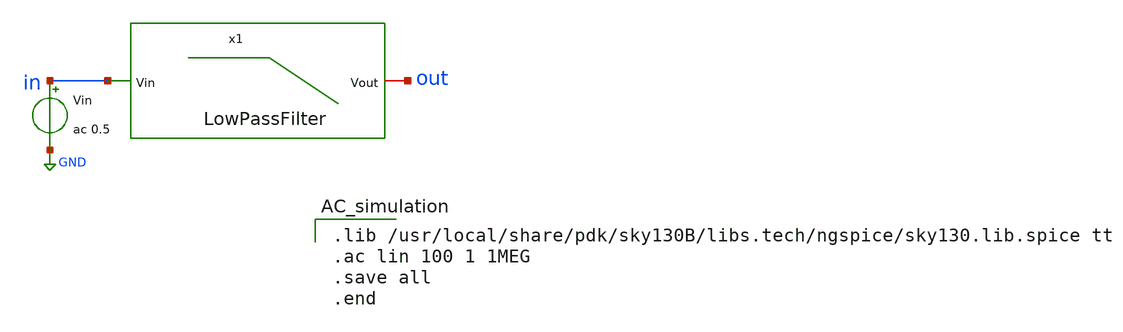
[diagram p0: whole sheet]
** sch_path: xschem/analog_desing/Filtro/LowPassFilter_tb.sch
**.subckt LowPassFilter_tb
x1 out in LowPassFilter
Vin in GND ac 0.5
**** begin user architecture code

.lib /usr/local/share/pdk/sky130B/libs.tech/ngspice/sky130.lib.spice tt
.ac lin 100 1 1MEG
.save all
.end

**** end user architecture code
**.ends

* expanding   symbol:  LowPassFilter.sym # of pins=2
** sym_path: xschem/analog_desing/Filtro/LowPassFilter.sym
** sch_path: xschem/analog_desing/Filtro/LowPassFilter.sch
.subckt LowPassFilter Vout Vin
*.ipin Vin
*.iopin Vout
XC1 Vout GND sky130_fd_pr__cap_mim_m3_1 W=1 L=1 MF=1 m=1
XR1 Vout Vin sky130_fd_pr__res_generic_po W=0.0503 L=10 m=1
.ends

.GLOBAL GND
.end
